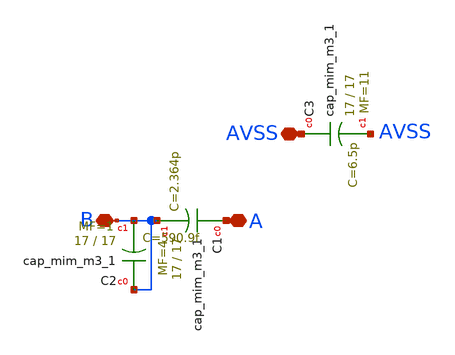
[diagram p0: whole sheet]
** sch_path: magic/cap_op.sch
**.subckt cap_op A B AVSS
*.iopin A
*.iopin B
*.iopin AVSS
XC1 A B sky130_fd_pr__cap_mim_m3_1 W=17 L=17 MF=4 m=4
XC2 B B sky130_fd_pr__cap_mim_m3_1 W=17 L=17 MF=1 m=1
XC3 AVSS AVSS sky130_fd_pr__cap_mim_m3_1 W=17 L=17 MF=11 m=11
**.ends
.end
